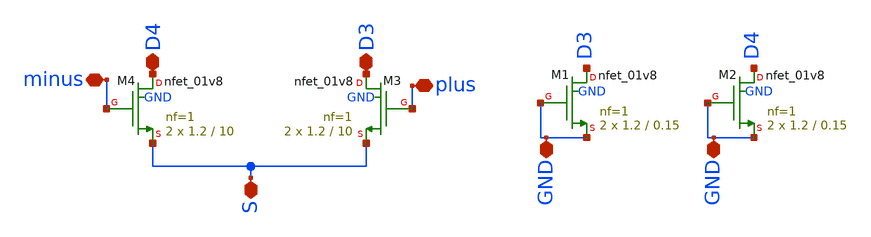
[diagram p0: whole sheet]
** sch_path: magic/diff_pair.sch
**.subckt diff_pair minus plus D4 D3 S GND GND
*.iopin minus
*.iopin plus
*.iopin D4
*.iopin D3
*.iopin S
*.iopin GND
*.iopin GND
XM3 D3 plus S GND sky130_fd_pr__nfet_01v8 L=10 W=1.2 nf=1 ad='int((nf+1)/2) * W/nf * 0.29' as='int((nf+2)/2) * W/nf * 0.29'
+ pd='2*int((nf+1)/2) * (W/nf + 0.29)' ps='2*int((nf+2)/2) * (W/nf + 0.29)' nrd='0.29 / W' nrs='0.29 / W'
+ sa=0 sb=0 sd=0 mult=2 m=2
XM4 D4 minus S GND sky130_fd_pr__nfet_01v8 L=10 W=1.2 nf=1 ad='int((nf+1)/2) * W/nf * 0.29' as='int((nf+2)/2) * W/nf * 0.29'
+ pd='2*int((nf+1)/2) * (W/nf + 0.29)' ps='2*int((nf+2)/2) * (W/nf + 0.29)' nrd='0.29 / W' nrs='0.29 / W'
+ sa=0 sb=0 sd=0 mult=2 m=2
XM1 D3 GND GND GND sky130_fd_pr__nfet_01v8 L=0.15 W=1.2 nf=1 ad='int((nf+1)/2) * W/nf * 0.29' as='int((nf+2)/2) * W/nf * 0.29'
+ pd='2*int((nf+1)/2) * (W/nf + 0.29)' ps='2*int((nf+2)/2) * (W/nf + 0.29)' nrd='0.29 / W' nrs='0.29 / W'
+ sa=0 sb=0 sd=0 mult=2 m=2
XM2 D4 GND GND GND sky130_fd_pr__nfet_01v8 L=0.15 W=1.2 nf=1 ad='int((nf+1)/2) * W/nf * 0.29' as='int((nf+2)/2) * W/nf * 0.29'
+ pd='2*int((nf+1)/2) * (W/nf + 0.29)' ps='2*int((nf+2)/2) * (W/nf + 0.29)' nrd='0.29 / W' nrs='0.29 / W'
+ sa=0 sb=0 sd=0 mult=2 m=2
**.ends
.end
